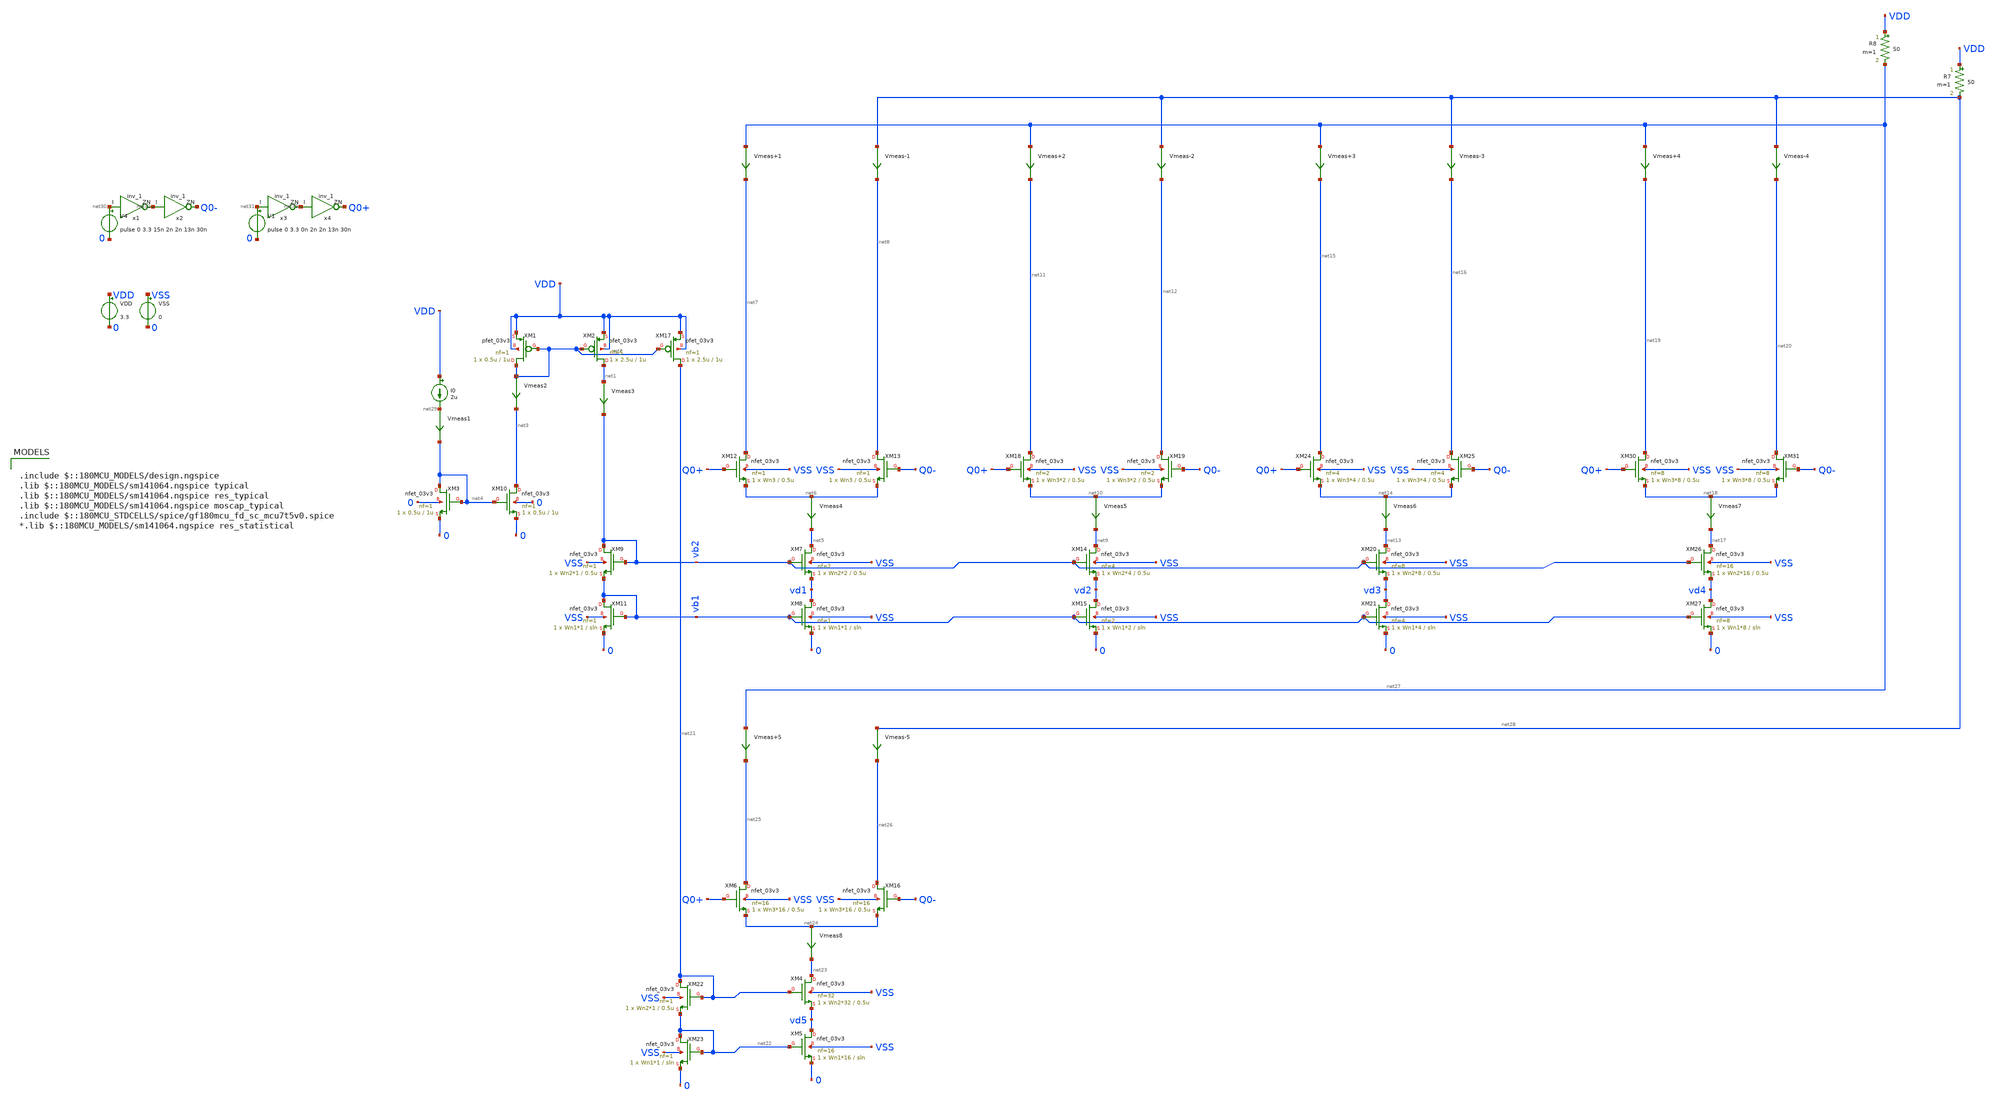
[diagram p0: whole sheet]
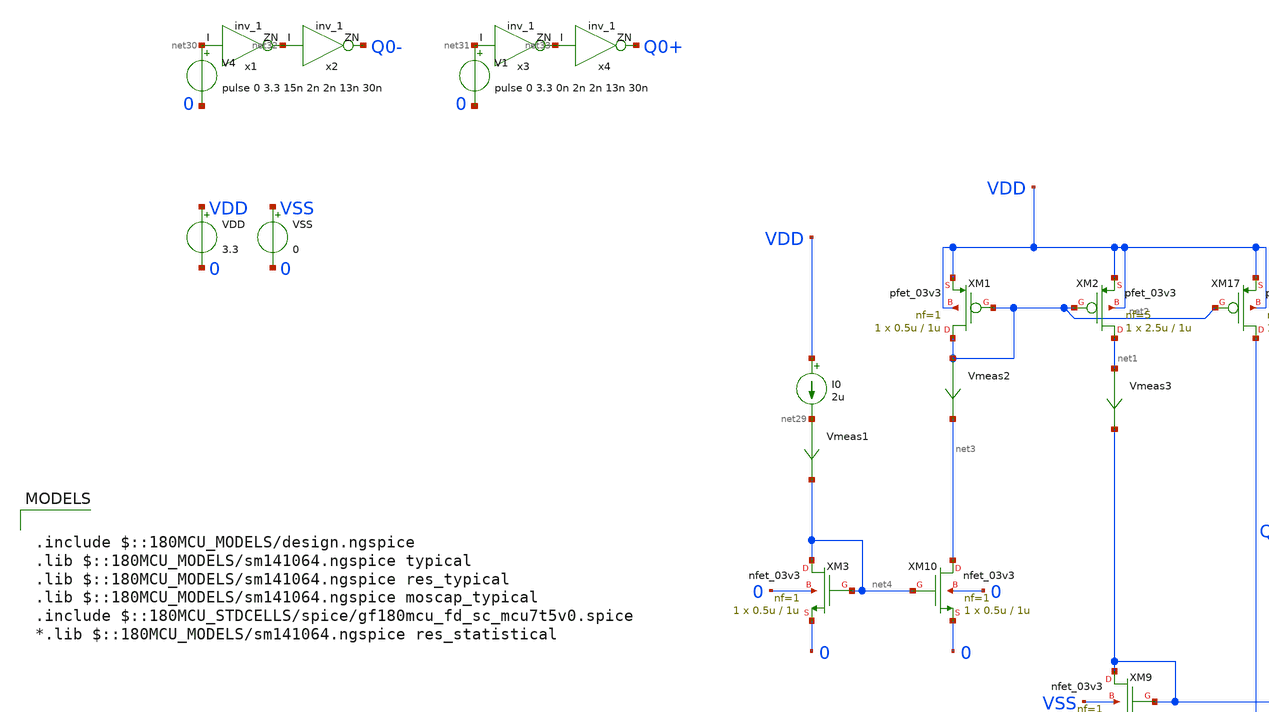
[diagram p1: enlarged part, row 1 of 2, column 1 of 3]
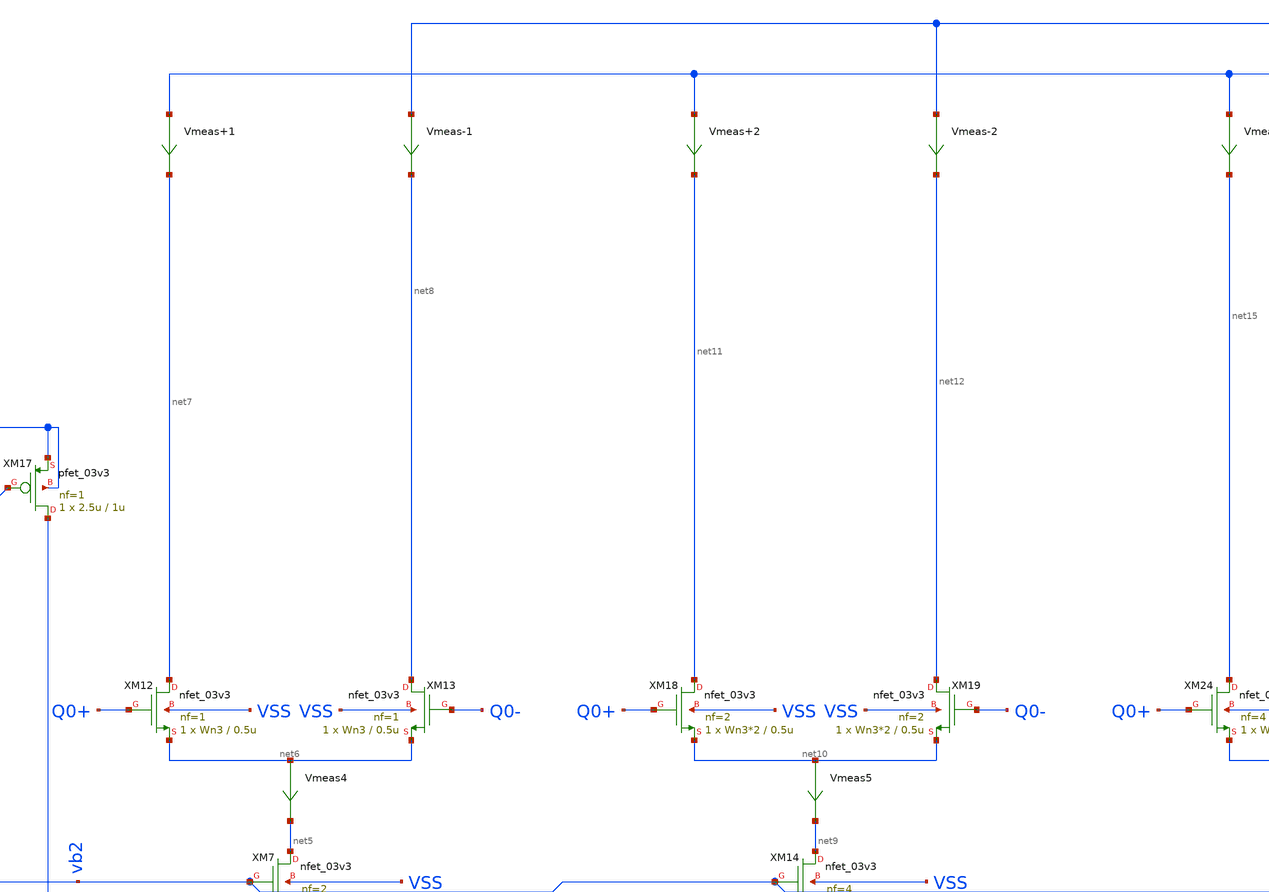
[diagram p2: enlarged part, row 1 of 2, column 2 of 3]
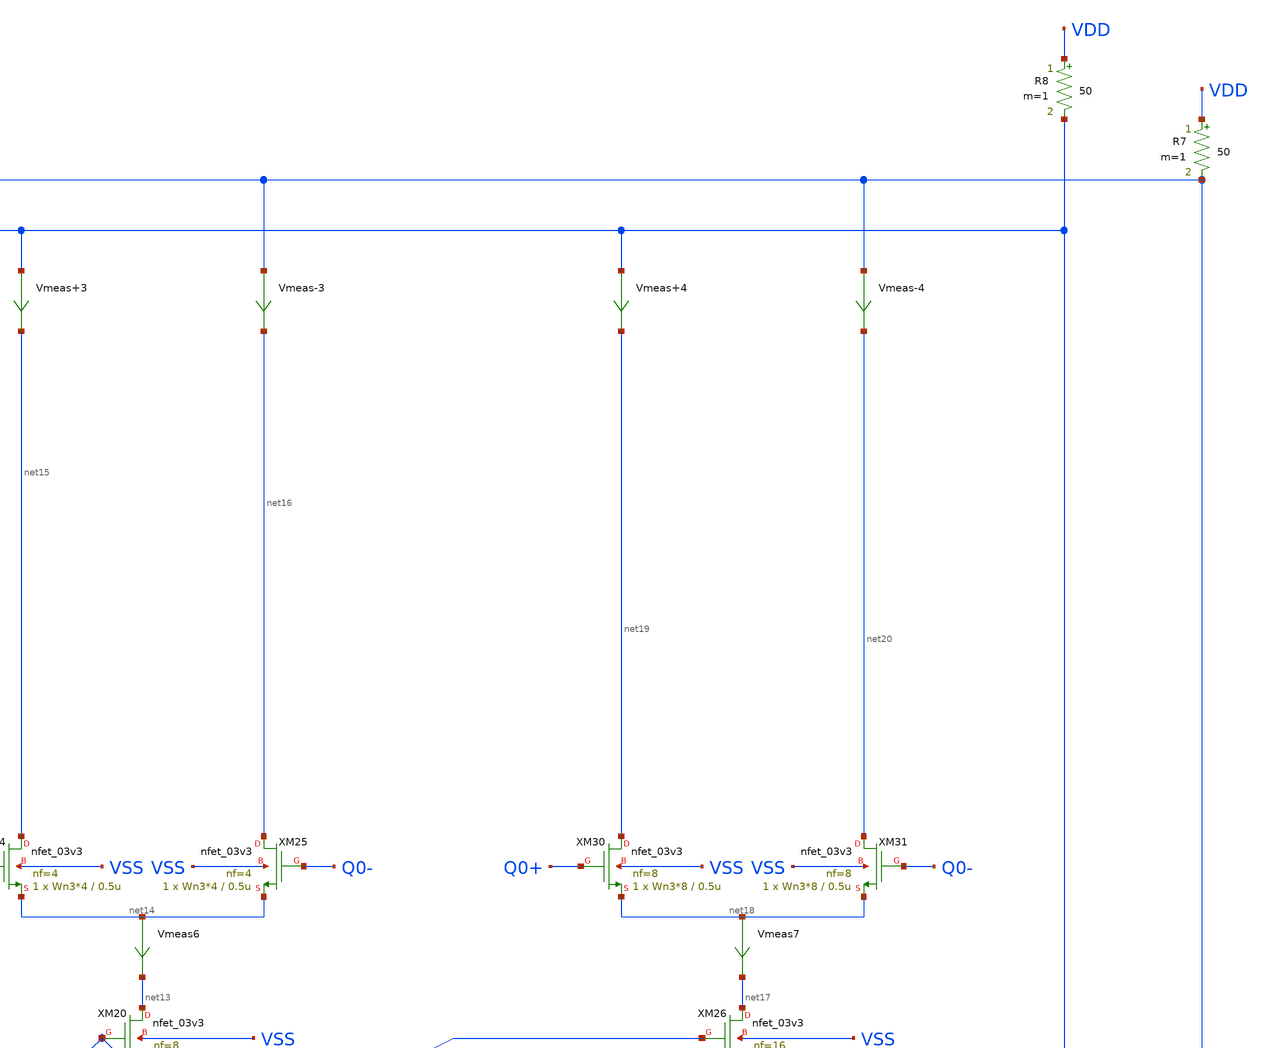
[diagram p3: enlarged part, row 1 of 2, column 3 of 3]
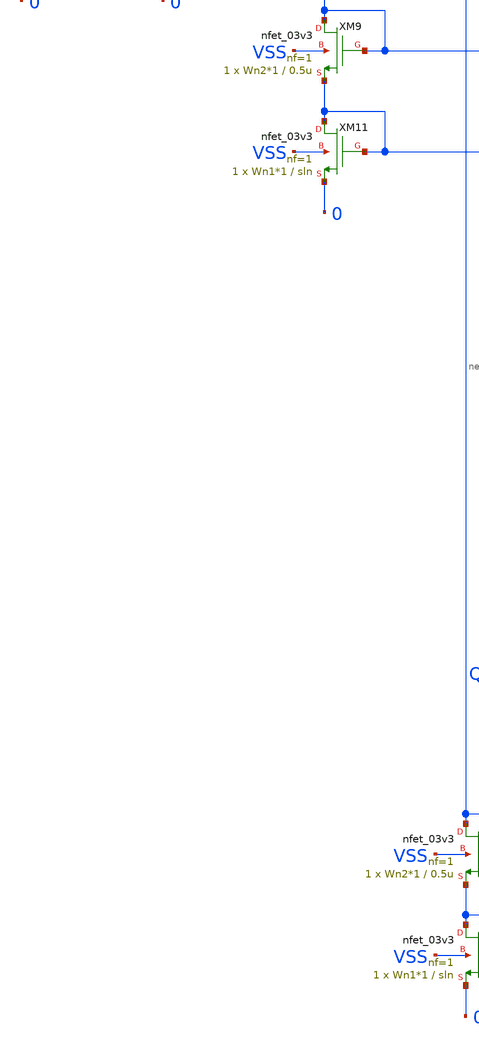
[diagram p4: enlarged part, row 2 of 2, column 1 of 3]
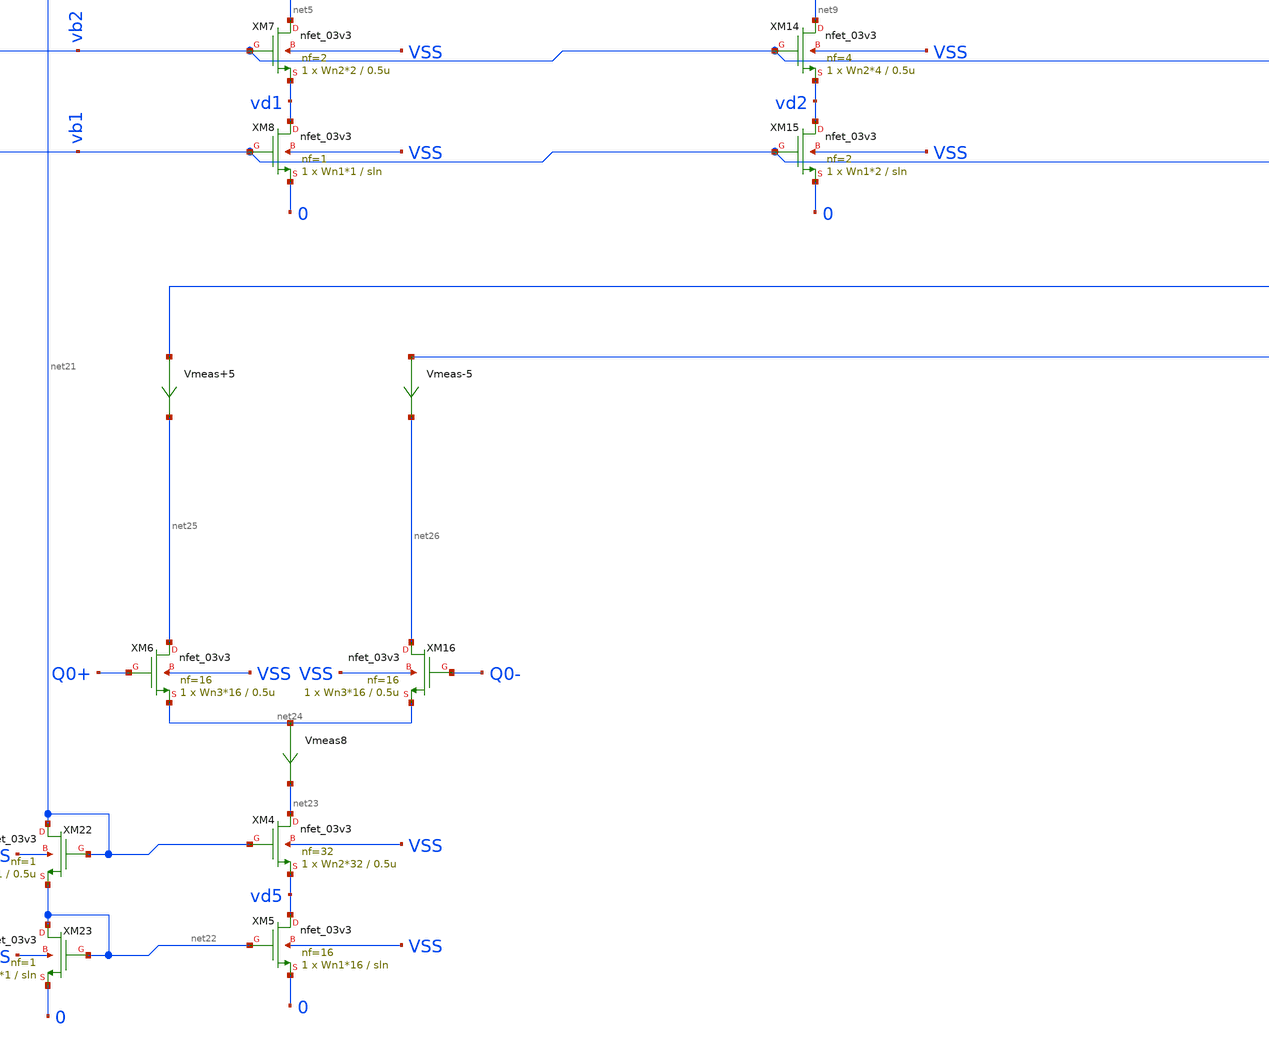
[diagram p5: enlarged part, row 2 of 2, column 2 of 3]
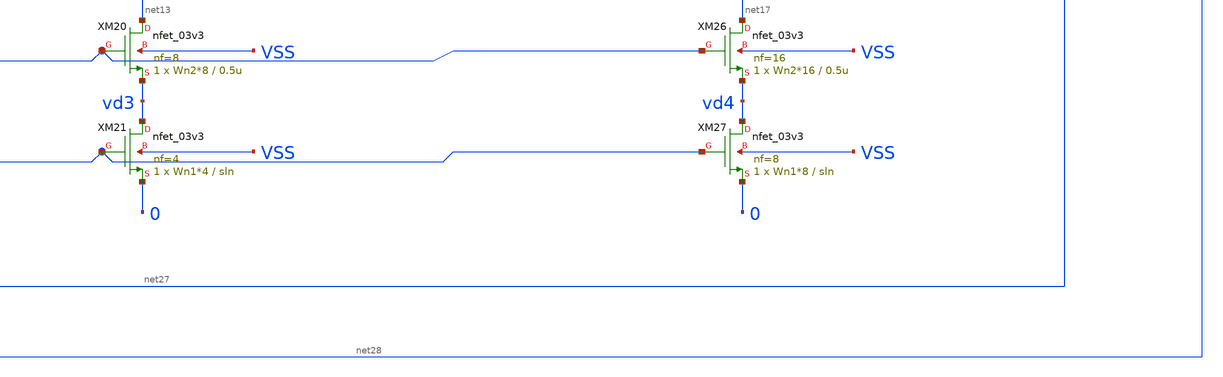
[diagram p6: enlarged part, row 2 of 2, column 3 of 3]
** sch_path: DAC/xschem/tb/tb_wl_vs_finger.sch
**.subckt tb_wl_vs_finger
XM1 net2 net2 VDD VDD pfet_03v3 L=1u W=0.5u nf=1 ad='int((nf+1)/2) * W/nf * 0.18u' as='int((nf+2)/2) * W/nf * 0.18u'
+ pd='2*int((nf+1)/2) * (W/nf + 0.18u)' ps='2*int((nf+2)/2) * (W/nf + 0.18u)' nrd='0.18u / W' nrs='0.18u / W'
+ sa=0 sb=0 sd=0 m=1
XM2 net1 net2 VDD VDD pfet_03v3 L=1u W=2.5u nf=5 ad='int((nf+1)/2) * W/nf * 0.18u' as='int((nf+2)/2) * W/nf * 0.18u'
+ pd='2*int((nf+1)/2) * (W/nf + 0.18u)' ps='2*int((nf+2)/2) * (W/nf + 0.18u)' nrd='0.18u / W' nrs='0.18u / W'
+ sa=0 sb=0 sd=0 m=1
I0 VDD net29 2u
XM3 net4 net4 0 0 nfet_03v3 L=1u W=0.5u nf=1 ad='int((nf+1)/2) * W/nf * 0.18u' as='int((nf+2)/2) * W/nf * 0.18u'
+ pd='2*int((nf+1)/2) * (W/nf + 0.18u)' ps='2*int((nf+2)/2) * (W/nf + 0.18u)' nrd='0.18u / W' nrs='0.18u / W'
+ sa=0 sb=0 sd=0 m=1
XM10 net3 net4 0 0 nfet_03v3 L=1u W=0.5u nf=1 ad='int((nf+1)/2) * W/nf * 0.18u' as='int((nf+2)/2) * W/nf * 0.18u'
+ pd='2*int((nf+1)/2) * (W/nf + 0.18u)' ps='2*int((nf+2)/2) * (W/nf + 0.18u)' nrd='0.18u / W' nrs='0.18u / W'
+ sa=0 sb=0 sd=0 m=1
Vmeas1 net29 net4 0
.save i(vmeas1)
XM7 net5 vb2 vd1 VSS nfet_03v3 L=0.5u W=Wn2*2 nf=2 ad='int((nf+1)/2) * W/nf * 0.18u' as='int((nf+2)/2) * W/nf * 0.18u'
+ pd='2*int((nf+1)/2) * (W/nf + 0.18u)' ps='2*int((nf+2)/2) * (W/nf + 0.18u)' nrd='0.18u / W' nrs='0.18u / W'
+ sa=0 sb=0 sd=0 m=1
XM8 vd1 vb1 0 VSS nfet_03v3 L=sln W=Wn1*1 nf=1 ad='int((nf+1)/2) * W/nf * 0.18u' as='int((nf+2)/2) * W/nf * 0.18u'
+ pd='2*int((nf+1)/2) * (W/nf + 0.18u)' ps='2*int((nf+2)/2) * (W/nf + 0.18u)' nrd='0.18u / W' nrs='0.18u / W'
+ sa=0 sb=0 sd=0 m=1
XM9 vb2 vb2 vb1 VSS nfet_03v3 L=0.5u W=Wn2*1 nf=1 ad='int((nf+1)/2) * W/nf * 0.18u' as='int((nf+2)/2) * W/nf * 0.18u'
+ pd='2*int((nf+1)/2) * (W/nf + 0.18u)' ps='2*int((nf+2)/2) * (W/nf + 0.18u)' nrd='0.18u / W' nrs='0.18u / W'
+ sa=0 sb=0 sd=0 m=1
XM11 vb1 vb1 0 VSS nfet_03v3 L=sln W=Wn1*1 nf=1 ad='int((nf+1)/2) * W/nf * 0.18u' as='int((nf+2)/2) * W/nf * 0.18u'
+ pd='2*int((nf+1)/2) * (W/nf + 0.18u)' ps='2*int((nf+2)/2) * (W/nf + 0.18u)' nrd='0.18u / W' nrs='0.18u / W'
+ sa=0 sb=0 sd=0 m=1
XM12 net7 Q0+ net6 VSS nfet_03v3 L=0.5u W=Wn3 nf=1 ad='int((nf+1)/2) * W/nf * 0.18u' as='int((nf+2)/2) * W/nf * 0.18u'
+ pd='2*int((nf+1)/2) * (W/nf + 0.18u)' ps='2*int((nf+2)/2) * (W/nf + 0.18u)' nrd='0.18u / W' nrs='0.18u / W'
+ sa=0 sb=0 sd=0 m=1
XM13 net8 Q0- net6 VSS nfet_03v3 L=0.5u W=Wn3 nf=1 ad='int((nf+1)/2) * W/nf * 0.18u' as='int((nf+2)/2) * W/nf * 0.18u'
+ pd='2*int((nf+1)/2) * (W/nf + 0.18u)' ps='2*int((nf+2)/2) * (W/nf + 0.18u)' nrd='0.18u / W' nrs='0.18u / W'
+ sa=0 sb=0 sd=0 m=1
Vmeas2 net2 net3 0
.save i(vmeas2)
Vmeas3 net1 vb2 0
.save i(vmeas3)
Vmeas4 net6 net5 0
.save i(vmeas4)
Vmeas+4 net27 net19 0
.save i(vmeas+4)
Vmeas-4 net28 net20 0
.save i(vmeas-4)
XM14 net9 vb2 vd2 VSS nfet_03v3 L=0.5u W=Wn2*4 nf=4 ad='int((nf+1)/2) * W/nf * 0.18u' as='int((nf+2)/2) * W/nf * 0.18u'
+ pd='2*int((nf+1)/2) * (W/nf + 0.18u)' ps='2*int((nf+2)/2) * (W/nf + 0.18u)' nrd='0.18u / W' nrs='0.18u / W'
+ sa=0 sb=0 sd=0 m=1
XM15 vd2 vb1 0 VSS nfet_03v3 L=sln W=Wn1*2 nf=2 ad='int((nf+1)/2) * W/nf * 0.18u' as='int((nf+2)/2) * W/nf * 0.18u'
+ pd='2*int((nf+1)/2) * (W/nf + 0.18u)' ps='2*int((nf+2)/2) * (W/nf + 0.18u)' nrd='0.18u / W' nrs='0.18u / W'
+ sa=0 sb=0 sd=0 m=1
XM18 net11 Q0+ net10 VSS nfet_03v3 L=0.5u W=Wn3*2 nf=2 ad='int((nf+1)/2) * W/nf * 0.18u' as='int((nf+2)/2) * W/nf * 0.18u'
+ pd='2*int((nf+1)/2) * (W/nf + 0.18u)' ps='2*int((nf+2)/2) * (W/nf + 0.18u)' nrd='0.18u / W' nrs='0.18u / W'
+ sa=0 sb=0 sd=0 m=1
XM19 net12 Q0- net10 VSS nfet_03v3 L=0.5u W=Wn3*2 nf=2 ad='int((nf+1)/2) * W/nf * 0.18u' as='int((nf+2)/2) * W/nf * 0.18u'
+ pd='2*int((nf+1)/2) * (W/nf + 0.18u)' ps='2*int((nf+2)/2) * (W/nf + 0.18u)' nrd='0.18u / W' nrs='0.18u / W'
+ sa=0 sb=0 sd=0 m=1
Vmeas+1 net27 net7 0
.save i(vmeas+1)
Vmeas-1 net28 net8 0
.save i(vmeas-1)
XM20 net13 vb2 vd3 VSS nfet_03v3 L=0.5u W=Wn2*8 nf=8 ad='int((nf+1)/2) * W/nf * 0.18u' as='int((nf+2)/2) * W/nf * 0.18u'
+ pd='2*int((nf+1)/2) * (W/nf + 0.18u)' ps='2*int((nf+2)/2) * (W/nf + 0.18u)' nrd='0.18u / W' nrs='0.18u / W'
+ sa=0 sb=0 sd=0 m=1
XM21 vd3 vb1 0 VSS nfet_03v3 L=sln W=Wn1*4 nf=4 ad='int((nf+1)/2) * W/nf * 0.18u' as='int((nf+2)/2) * W/nf * 0.18u'
+ pd='2*int((nf+1)/2) * (W/nf + 0.18u)' ps='2*int((nf+2)/2) * (W/nf + 0.18u)' nrd='0.18u / W' nrs='0.18u / W'
+ sa=0 sb=0 sd=0 m=1
XM24 net15 Q0+ net14 VSS nfet_03v3 L=0.5u W=Wn3*4 nf=4 ad='int((nf+1)/2) * W/nf * 0.18u' as='int((nf+2)/2) * W/nf * 0.18u'
+ pd='2*int((nf+1)/2) * (W/nf + 0.18u)' ps='2*int((nf+2)/2) * (W/nf + 0.18u)' nrd='0.18u / W' nrs='0.18u / W'
+ sa=0 sb=0 sd=0 m=1
XM25 net16 Q0- net14 VSS nfet_03v3 L=0.5u W=Wn3*4 nf=4 ad='int((nf+1)/2) * W/nf * 0.18u' as='int((nf+2)/2) * W/nf * 0.18u'
+ pd='2*int((nf+1)/2) * (W/nf + 0.18u)' ps='2*int((nf+2)/2) * (W/nf + 0.18u)' nrd='0.18u / W' nrs='0.18u / W'
+ sa=0 sb=0 sd=0 m=1
XM26 net17 vb2 vd4 VSS nfet_03v3 L=0.5u W=Wn2*16 nf=16 ad='int((nf+1)/2) * W/nf * 0.18u' as='int((nf+2)/2) * W/nf * 0.18u'
+ pd='2*int((nf+1)/2) * (W/nf + 0.18u)' ps='2*int((nf+2)/2) * (W/nf + 0.18u)' nrd='0.18u / W' nrs='0.18u / W'
+ sa=0 sb=0 sd=0 m=1
XM27 vd4 vb1 0 VSS nfet_03v3 L=sln W=Wn1*8 nf=8 ad='int((nf+1)/2) * W/nf * 0.18u' as='int((nf+2)/2) * W/nf * 0.18u'
+ pd='2*int((nf+1)/2) * (W/nf + 0.18u)' ps='2*int((nf+2)/2) * (W/nf + 0.18u)' nrd='0.18u / W' nrs='0.18u / W'
+ sa=0 sb=0 sd=0 m=1
XM30 net19 Q0+ net18 VSS nfet_03v3 L=0.5u W=Wn3*8 nf=8 ad='int((nf+1)/2) * W/nf * 0.18u' as='int((nf+2)/2) * W/nf * 0.18u'
+ pd='2*int((nf+1)/2) * (W/nf + 0.18u)' ps='2*int((nf+2)/2) * (W/nf + 0.18u)' nrd='0.18u / W' nrs='0.18u / W'
+ sa=0 sb=0 sd=0 m=1
XM31 net20 Q0- net18 VSS nfet_03v3 L=0.5u W=Wn3*8 nf=8 ad='int((nf+1)/2) * W/nf * 0.18u' as='int((nf+2)/2) * W/nf * 0.18u'
+ pd='2*int((nf+1)/2) * (W/nf + 0.18u)' ps='2*int((nf+2)/2) * (W/nf + 0.18u)' nrd='0.18u / W' nrs='0.18u / W'
+ sa=0 sb=0 sd=0 m=1
Vmeas+2 net27 net11 0
.save i(vmeas+2)
Vmeas-2 net28 net12 0
.save i(vmeas-2)
R7 VDD net28 50 m=1
R8 VDD net27 50 m=1
Vmeas+3 net27 net15 0
.save i(vmeas+3)
Vmeas-3 net28 net16 0
.save i(vmeas-3)
VDD VDD 0 3.3
VSS VSS 0 0
V4 net30 0 pulse 0 3.3 15n 2n 2n 13n 30n
V1 net31 0 pulse 0 3.3 0n 2n 2n 13n 30n
x1 net30 net32 VDD VNW VPW VSS gf180mcu_fd_sc_mcu7t5v0__inv_1
x2 net32 Q0- VDD VNW VPW VSS gf180mcu_fd_sc_mcu7t5v0__inv_1
x3 net31 net33 VDD VNW VPW VSS gf180mcu_fd_sc_mcu7t5v0__inv_1
x4 net33 Q0+ VDD VNW VPW VSS gf180mcu_fd_sc_mcu7t5v0__inv_1
Vmeas+5 net27 net25 0
.save i(vmeas+5)
Vmeas-5 net28 net26 0
.save i(vmeas-5)
XM4 net23 net21 vd5 VSS nfet_03v3 L=0.5u W=Wn2*32 nf=32 ad='int((nf+1)/2) * W/nf * 0.18u' as='int((nf+2)/2) * W/nf * 0.18u'
+ pd='2*int((nf+1)/2) * (W/nf + 0.18u)' ps='2*int((nf+2)/2) * (W/nf + 0.18u)' nrd='0.18u / W' nrs='0.18u / W'
+ sa=0 sb=0 sd=0 m=1
XM5 vd5 net22 0 VSS nfet_03v3 L=sln W=Wn1*16 nf=16 ad='int((nf+1)/2) * W/nf * 0.18u' as='int((nf+2)/2) * W/nf * 0.18u'
+ pd='2*int((nf+1)/2) * (W/nf + 0.18u)' ps='2*int((nf+2)/2) * (W/nf + 0.18u)' nrd='0.18u / W' nrs='0.18u / W'
+ sa=0 sb=0 sd=0 m=1
XM6 net25 Q0+ net24 VSS nfet_03v3 L=0.5u W=Wn3*16 nf=16 ad='int((nf+1)/2) * W/nf * 0.18u' as='int((nf+2)/2) * W/nf * 0.18u'
+ pd='2*int((nf+1)/2) * (W/nf + 0.18u)' ps='2*int((nf+2)/2) * (W/nf + 0.18u)' nrd='0.18u / W' nrs='0.18u / W'
+ sa=0 sb=0 sd=0 m=1
XM16 net26 Q0- net24 VSS nfet_03v3 L=0.5u W=Wn3*16 nf=16 ad='int((nf+1)/2) * W/nf * 0.18u' as='int((nf+2)/2) * W/nf * 0.18u'
+ pd='2*int((nf+1)/2) * (W/nf + 0.18u)' ps='2*int((nf+2)/2) * (W/nf + 0.18u)' nrd='0.18u / W' nrs='0.18u / W'
+ sa=0 sb=0 sd=0 m=1
XM17 net21 net2 VDD VDD pfet_03v3 L=1u W=2.5u nf=1 ad='int((nf+1)/2) * W/nf * 0.18u' as='int((nf+2)/2) * W/nf * 0.18u'
+ pd='2*int((nf+1)/2) * (W/nf + 0.18u)' ps='2*int((nf+2)/2) * (W/nf + 0.18u)' nrd='0.18u / W' nrs='0.18u / W'
+ sa=0 sb=0 sd=0 m=1
XM22 net21 net21 net22 VSS nfet_03v3 L=0.5u W=Wn2*1 nf=1 ad='int((nf+1)/2) * W/nf * 0.18u' as='int((nf+2)/2) * W/nf * 0.18u'
+ pd='2*int((nf+1)/2) * (W/nf + 0.18u)' ps='2*int((nf+2)/2) * (W/nf + 0.18u)' nrd='0.18u / W' nrs='0.18u / W'
+ sa=0 sb=0 sd=0 m=1
XM23 net22 net22 0 VSS nfet_03v3 L=sln W=Wn1*1 nf=1 ad='int((nf+1)/2) * W/nf * 0.18u' as='int((nf+2)/2) * W/nf * 0.18u'
+ pd='2*int((nf+1)/2) * (W/nf + 0.18u)' ps='2*int((nf+2)/2) * (W/nf + 0.18u)' nrd='0.18u / W' nrs='0.18u / W'
+ sa=0 sb=0 sd=0 m=1
Vmeas5 net10 net9 0
.save i(vmeas5)
Vmeas6 net14 net13 0
.save i(vmeas6)
Vmeas7 net18 net17 0
.save i(vmeas7)
Vmeas8 net24 net23 0
.save i(vmeas8)
**** begin user architecture code


.param Mn1=1
.param Mn2=1
.param Mn3=1
.param Mn4=1
.param nf1=1
.param nf2=2
.param nf3=3
.param nf4=4
.param sln=4u
.param Wn1=8u
*.param Wn11=1u
.param Wn11=1.85u
.param Wn2=1u
*.param Wn22=1u
.param Wn22=0.9u
.param Wn3=1u
.save @m.xm7.m0[vth] @m.xm8.m0[vth] @m.xm27.m0[vth] @m.xm26.m0[vth] @m.xm30.m0[vth]
.options savecurrents

.control
	tran 0.5n 100n
	*plot i(Vmeas1) i(Vmeas2) i(Vmeas3) i(Vmeas4) i(Vmeas5)
	*plot v(vb2) v(vb1) v(vd1) v(vd2)
	plot i(Vmeas+1) i(Vmeas-1) i(Vmeas+2) i(Vmeas-2) i(Vmeas+3) i(Vmeas-3) i(Vmeas+4) i(Vmeas-4)
+ i(Vmeas+5) i(Vmeas-5)
	plot v(vb1)-@m.xm8.m0[vth]
	plot v(vb2)-v(vd1)-@m.xm7.m0[vth]
	*plot v(vb1)-@m.xm8.m0[vth]
	*plot v(vb2)-v(vd1)-@m.xm7.m0[vth]
	*plot v(q0+)-v(vd2)-@m.xm12.m0[vth]
	*plot v(vb1)-@m.xm27.m0[vth]
	*plot v(q0+)-v(vd2)-@m.xm12.m0[vth]
	plot @m.xm8.m0[vth] @m.xm27.m0[vth]
	plot v(vd1)-v(vb1)+@m.xm8.m0[vth]
	plot v(vd1)-v(vb1)+@m.xm15.m0[vth]
	plot v(vd1)-v(vb1)+@m.xm21.m0[vth]
	plot v(vd1)-v(vb1)+@m.xm27.m0[vth]
	plot v(vd1)-v(vb1)+@m.xm5.m0[vth]
	plot v(vd1) v(vd2) v(vd3) v(vd4) v(vd5)
	plot i(vmeas4) i(vmeas5) i(vmeas6) i(vmeas7) i(vmeas8)
	write test_finger.raw
.endc

.save all



.include $::180MCU_MODELS/design.ngspice
.lib $::180MCU_MODELS/sm141064.ngspice typical
.lib $::180MCU_MODELS/sm141064.ngspice res_typical
.lib $::180MCU_MODELS/sm141064.ngspice moscap_typical
.include $::180MCU_STDCELLS/spice/gf180mcu_fd_sc_mcu7t5v0.spice
*.lib $::180MCU_MODELS/sm141064.ngspice res_statistical

**** end user architecture code
**.ends
.end
